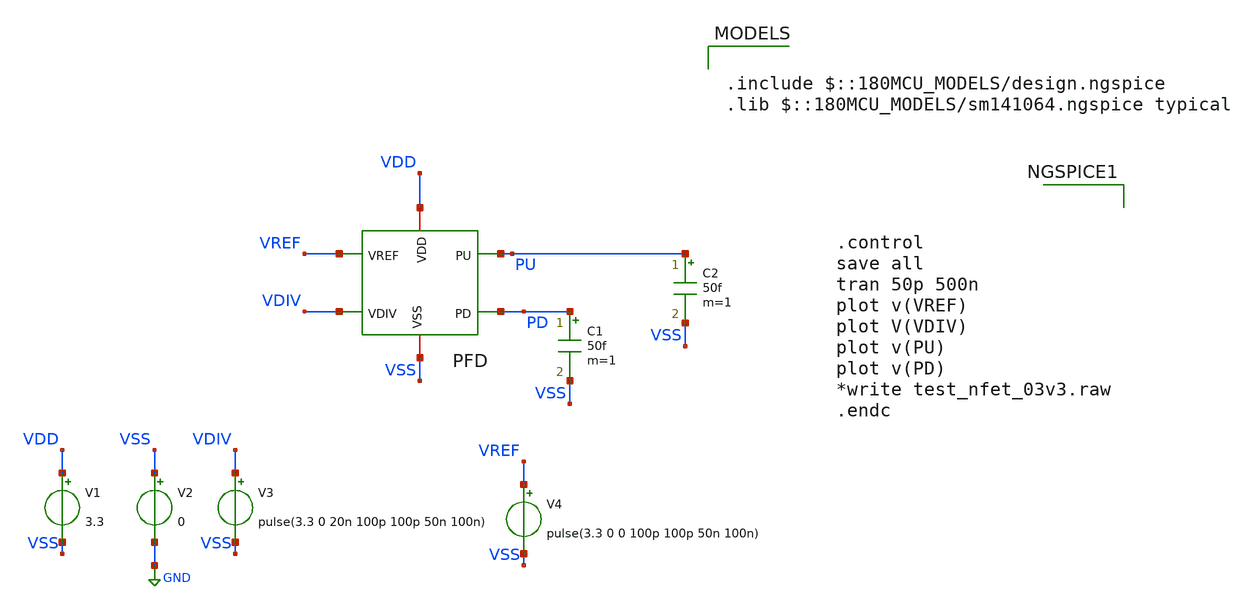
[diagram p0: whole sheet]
** sch_path: Clock_Generator_PAKISTAN_02/xschem/test_PFD.sch
**.subckt test_PFD
x1 VSS VREF VDIV PU PD VDD PFD
V1 VDD VSS 3.3
V2 VSS GND 0
V3 VDIV VSS pulse(3.3 0 20n 100p 100p 50n 100n)
V4 VREF VSS pulse(3.3 0 0 100p 100p 50n 100n)
C1 PD VSS 50f m=1
C2 PU VSS 50f m=1
**** begin user architecture code

.include $::180MCU_MODELS/design.ngspice
.lib $::180MCU_MODELS/sm141064.ngspice typical




.control
save all
tran 50p 500n
plot v(VREF)
plot V(VDIV)
plot v(PU)
plot v(PD)
*write test_nfet_03v3.raw
.endc


**** end user architecture code
**.ends
.GLOBAL GND
.end
